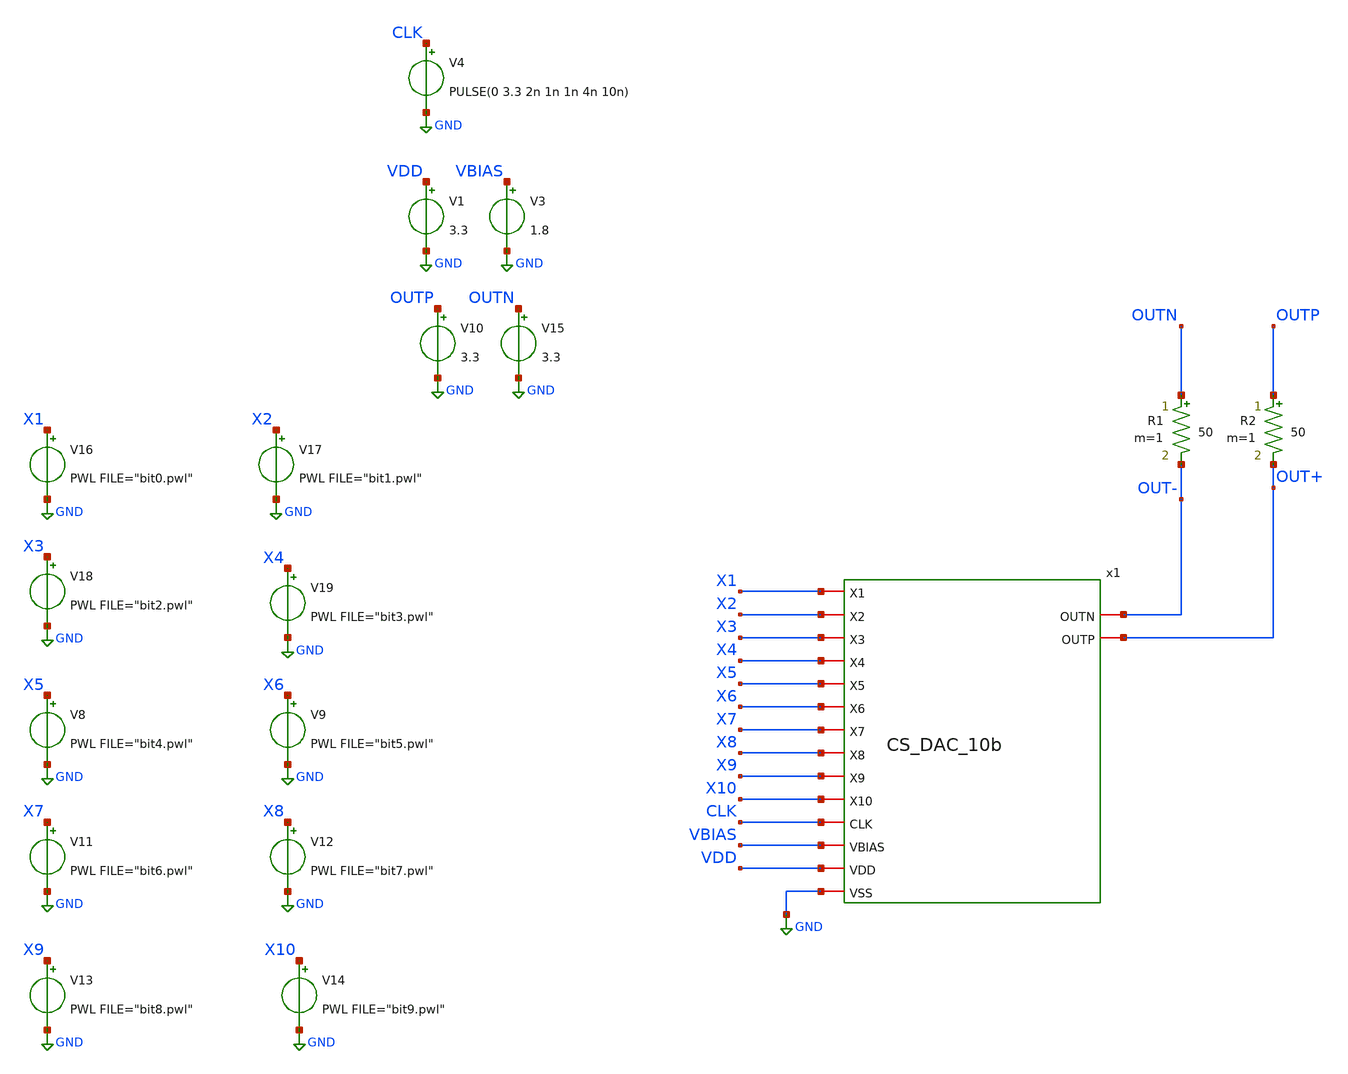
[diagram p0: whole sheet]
** sch_path: xschem/Test_data.sch
**.subckt Test_data
x1 X1 X2 X3 X4 X5 X6 X7 X8 X9 X10 CLK OUT+ OUT- VBIAS VDD GND CS_DAC_10b
V4 CLK GND PULSE(0 3.3 2n 1n 1n 4n 10n)
V8 X5 GND PWL FILE="bit4.pwl"
V9 X6 GND PWL FILE="bit5.pwl"
V11 X7 GND PWL FILE="bit6.pwl"
V12 X8 GND PWL FILE="bit7.pwl"
V13 X9 GND PWL FILE="bit8.pwl"
V14 X10 GND PWL FILE="bit9.pwl"
V1 VDD GND 3.3
V3 VBIAS GND 1.8
R1 OUTN OUT- 50 m=1
V10 OUTP GND 3.3
V15 OUTN GND 3.3
V16 X1 GND PWL FILE="bit0.pwl"
V17 X2 GND PWL FILE="bit1.pwl"
V18 X3 GND PWL FILE="bit2.pwl"
V19 X4 GND PWL FILE="bit3.pwl"
R2 OUTP OUT+ 50 m=1
**** begin user architecture code


.save @R1[i] @R2[i] v(OUT+) v(OUT-) v(CLK)

.control
set wr_vecnames
set wr_singlescale
tran 1n 5120n
wrdata /home/lecongmanh/CS_DAC/spice/CS_DAC_10b2.txt @R1[i] @R2[i] v(OUT+) v(OUT-) v(CLK)

.endc



.include /home/lecongmanh/conda-gf180mcu-env/envs/gf180mcu-env/share/pdk/gf180mcuD/libs.tech/ngspice/design.ngspice
.lib /home/lecongmanh/conda-gf180mcu-env/envs/gf180mcu-env/share/pdk/gf180mcuD/libs.tech/ngspice/sm141064.ngspice typical
.lib /home/lecongmanh/conda-gf180mcu-env/envs/gf180mcu-env/share/pdk/gf180mcuD/libs.tech/ngspice/smbb000149.ngspice typical

.include /home/lecongmanh/conda-gf180mcu-env/envs/gf180mcu-env/share/pdk/gf180mcuD/libs.ref/gf180mcu_fd_sc_mcu7t5v0/spice/gf180mcu_fd_sc_mcu7t5v0.spice

**** end user architecture code
**.ends
.GLOBAL GND
.end
